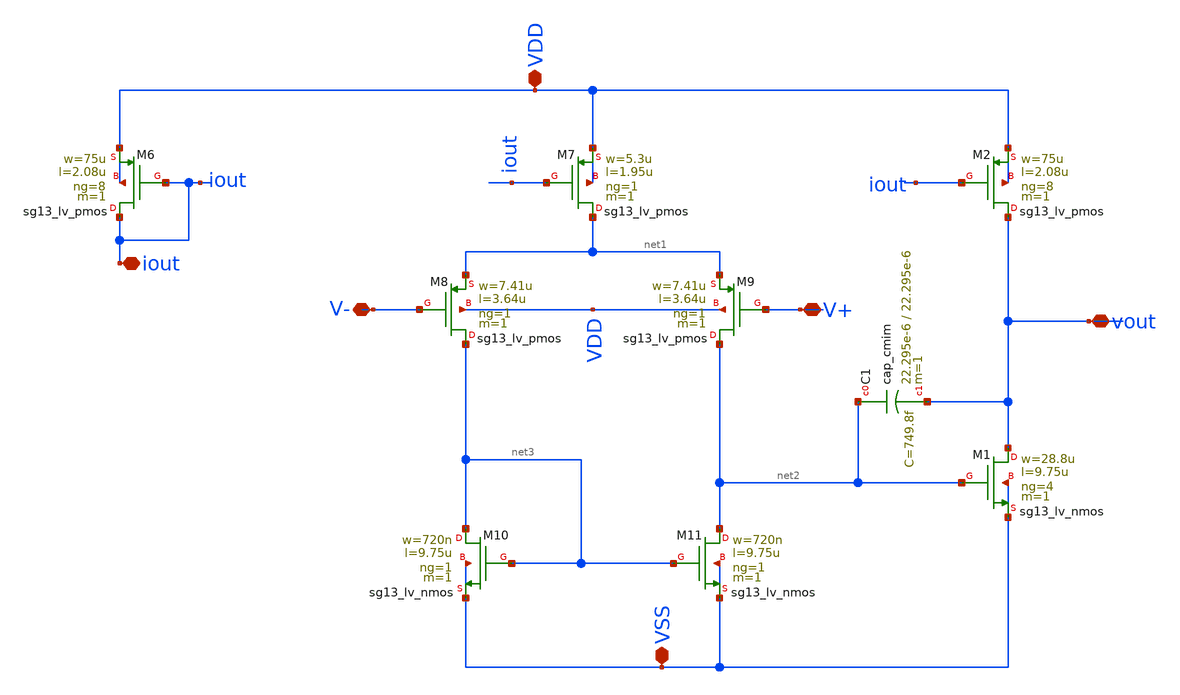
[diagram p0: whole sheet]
** sch_path: BTDay7-Ex/OTA.sch
**.subckt OTA VDD iout V- VSS V+ vout
*.iopin VDD
*.iopin iout
*.iopin V-
*.iopin VSS
*.iopin V+
*.iopin vout
XM6 iout iout VDD VDD sg13_lv_pmos w=75u l=2.08u ng=8 m=1 mm_ok=1
XM7 net1 iout VDD VDD sg13_lv_pmos w=5.3u l=1.95u ng=1 m=1 mm_ok=1
XM8 net3 V- net1 VDD sg13_lv_pmos w=7.41u l=3.64u ng=1 m=1 mm_ok=1
XM9 net2 V+ net1 VDD sg13_lv_pmos w=7.41u l=3.64u ng=1 m=1 mm_ok=1
XM10 net3 net3 VSS VSS sg13_lv_nmos w=720n l=9.75u ng=1 m=1 mm_ok=1
XM11 net2 net3 VSS VSS sg13_lv_nmos w=720n l=9.75u ng=1 m=1 mm_ok=1
XM1 vout net2 VSS VSS sg13_lv_nmos w=28.8u l=9.75u ng=4 m=1 mm_ok=1
XM2 vout iout VDD VDD sg13_lv_pmos w=75u l=2.08u ng=8 m=1 mm_ok=1
XC1 net2 vout cap_cmim w=22.295e-6 l=22.295e-6 m=1 mm_ok=1
**.ends
.end
